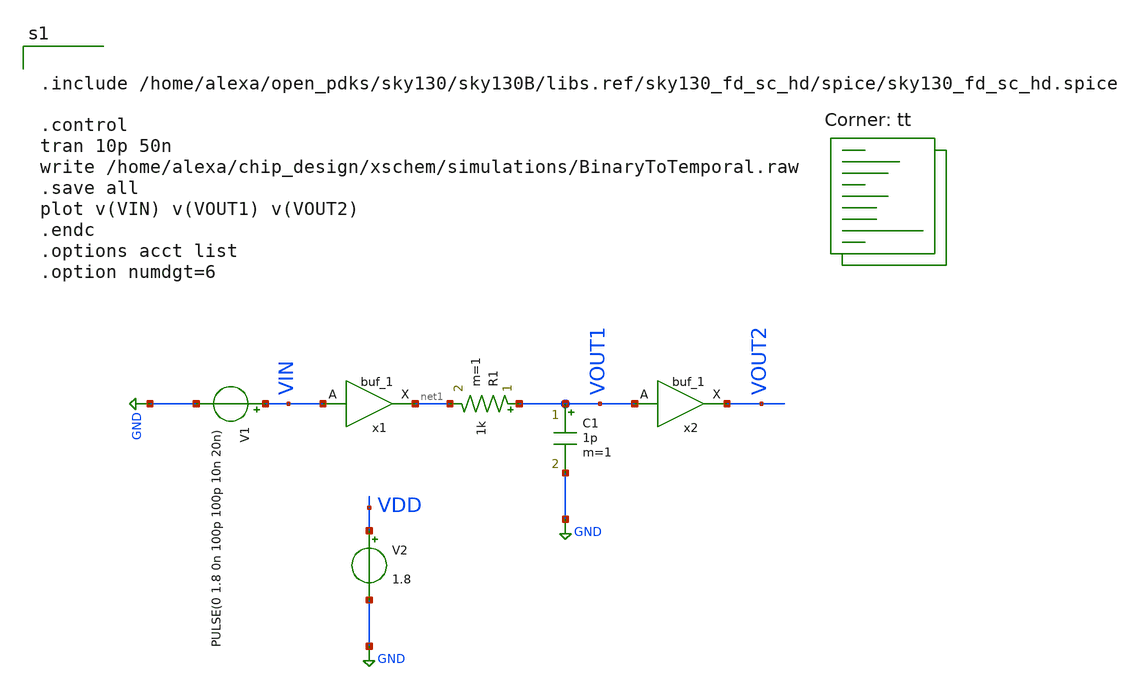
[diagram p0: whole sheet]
** sch_path: xschem/projects/BinToTemp.sch
**.subckt BinToTemp
R1 VOUT1 net1 1k m=1
C1 VOUT1 GND 1p m=1
V1 VIN GND PULSE(0 1.8 0n 100p 100p 10n 20n)
V2 VDD GND 1.8
x1 VIN 0 0 VDD VDD net1 sky130_fd_sc_hd__buf_1
x2 VOUT1 0 0 VDD VDD VOUT2 sky130_fd_sc_hd__buf_1
**** begin user architecture code


.include /home/alexa/open_pdks/sky130/sky130B/libs.ref/sky130_fd_sc_hd/spice/sky130_fd_sc_hd.spice

.control
tran 10p 50n
write /home/alexa/chip_design/xschem/simulations/BinaryToTemporal.raw
.save all
plot v(VIN) v(VOUT1) v(VOUT2)
.endc
.options acct list
.option numdgt=6


.lib $::SKYWATER_MODELS/sky130.lib.spice tt
**** end user architecture code
**.ends
.GLOBAL GND
.end
